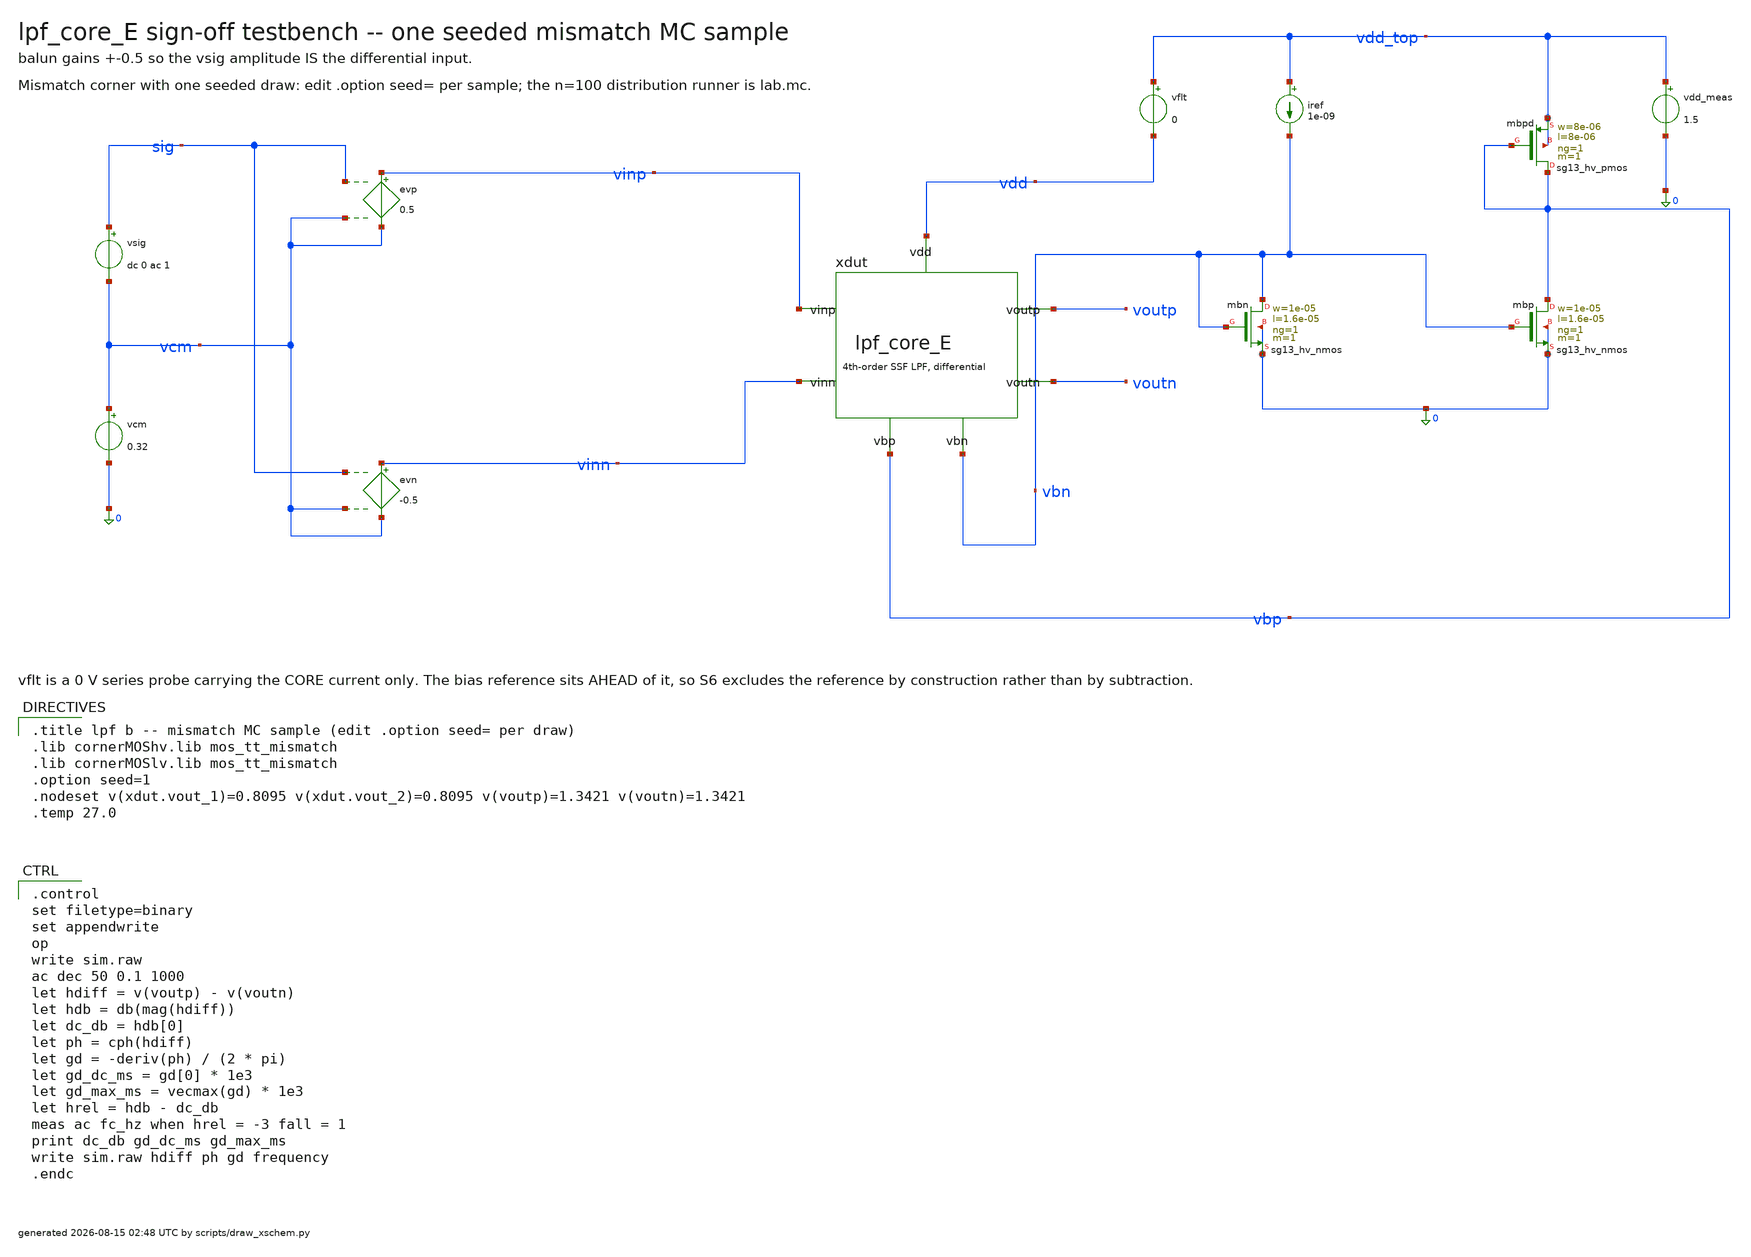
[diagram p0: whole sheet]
** sch_path: signoff/pre-pvt/E-combo/lpf_tb_E_mc.sch
**.subckt lpf_tb_E_mc
vsig sig vcm dc 0 ac 1
vcm vcm 0 0.32
evp vinp vcm sig vcm 0.5
evn vinn vcm sig vcm -0.5
xdut vinp vinn voutp voutn vbn vbp vdd lpf_core_E
vflt vdd_top vdd 0
vdd_meas vdd_top 0 1.5
iref vdd_top vbn 1e-09
Xmbn vbn vbn 0 0 sg13_hv_nmos w=1e-05 l=1.6e-05 ng=1 m=1 mm_ok=1
Xmbp vbp vbn 0 0 sg13_hv_nmos w=1e-05 l=1.6e-05 ng=1 m=1 mm_ok=1
Xmbpd vbp vbp vdd_top vdd_top sg13_hv_pmos w=8e-06 l=8e-06 ng=1 m=1 mm_ok=1
**** begin user architecture code

.title lpf b -- mismatch MC sample (edit .option seed= per draw)
.lib cornerMOShv.lib mos_tt_mismatch
.lib cornerMOSlv.lib mos_tt_mismatch
.option seed=1
.nodeset v(xdut.vout_1)=0.8095 v(xdut.vout_2)=0.8095 v(voutp)=1.3421 v(voutn)=1.3421
.temp 27.0


.control
set filetype=binary
set appendwrite
op
write sim.raw
ac dec 50 0.1 1000
let hdiff = v(voutp) - v(voutn)
let hdb = db(mag(hdiff))
let dc_db = hdb[0]
let ph = cph(hdiff)
let gd = -deriv(ph) / (2 * pi)
let gd_dc_ms = gd[0] * 1e3
let gd_max_ms = vecmax(gd) * 1e3
let hrel = hdb - dc_db
meas ac fc_hz when hrel = -3 fall = 1
print dc_db gd_dc_ms gd_max_ms
write sim.raw hdiff ph gd frequency
.endc

**** end user architecture code
**.ends

* expanding   symbol:  lpf_core_E.sym # of pins=7
** sym_path: signoff/E-combo/lpf_core_E.sym
** sch_path: signoff/E-combo/lpf_core_E.sch
.subckt lpf_core_E vinp vinn voutp voutn vbn vbp vdd
*.ipin vinp
*.ipin vinn
*.opin voutp
*.opin voutn
*.ipin vdd
*.ipin vbn
*.ipin vbp
Xm2 net2 vinp vout_1 vout_1 sg13_hv_pmos w=8e-06 l=8e-06 ng=1 m=1 mm_ok=1
Xm5 net3 vinn vout_2 vout_2 sg13_hv_pmos w=8e-06 l=8e-06 ng=1 m=1 mm_ok=1
Xm4 vout_1 net2 0 0 sg13_hv_nmos w=1e-06 l=4.5e-05 ng=1 m=1 mm_ok=1
Xm8 vout_2 net3 0 0 sg13_hv_nmos w=1e-06 l=4.5e-05 ng=1 m=1 mm_ok=1
Xm9 net2 vbn 0 0 sg13_hv_nmos w=1e-05 l=1.6e-05 ng=1 m=1 mm_ok=1
Xm10 net3 vbn 0 0 sg13_hv_nmos w=1e-05 l=1.6e-05 ng=1 m=1 mm_ok=1
Xmst vout_1 vbn net4 net4 sg13_hv_pmos w=4.8e-07 l=3.36e-05 ng=1 m=1 mm_ok=1
Xmstn vout_2 vbn net1 net1 sg13_hv_pmos w=4.8e-07 l=3.36e-05 ng=1 m=1 mm_ok=1
Xm0 net4 vout_1 voutp voutp sg13_hv_pmos w=8e-06 l=8e-06 ng=1 m=1 mm_ok=1
Xm1 net1 vout_2 voutn voutn sg13_hv_pmos w=8e-06 l=8e-06 ng=1 m=1 mm_ok=1
Xm14 voutp net4 vdd vdd sg13_lv_pmos w=1.28e-06 l=9.6e-05 ng=1 m=1 mm_ok=1
Xm15 voutn net1 vdd vdd sg13_lv_pmos w=1.28e-06 l=9.6e-05 ng=1 m=1 mm_ok=1
c13 net2 vout_1 8.61884e-12 m=1
c17 net3 vout_2 8.61884e-12 m=1
c19 vout_2 vout_1 2.36443e-11 m=1
c1 voutp net4 8.10786e-11 m=1
c10 voutn net1 8.10786e-11 m=1
c12 voutn voutp 1.69787e-11 m=1
.ends

.end
